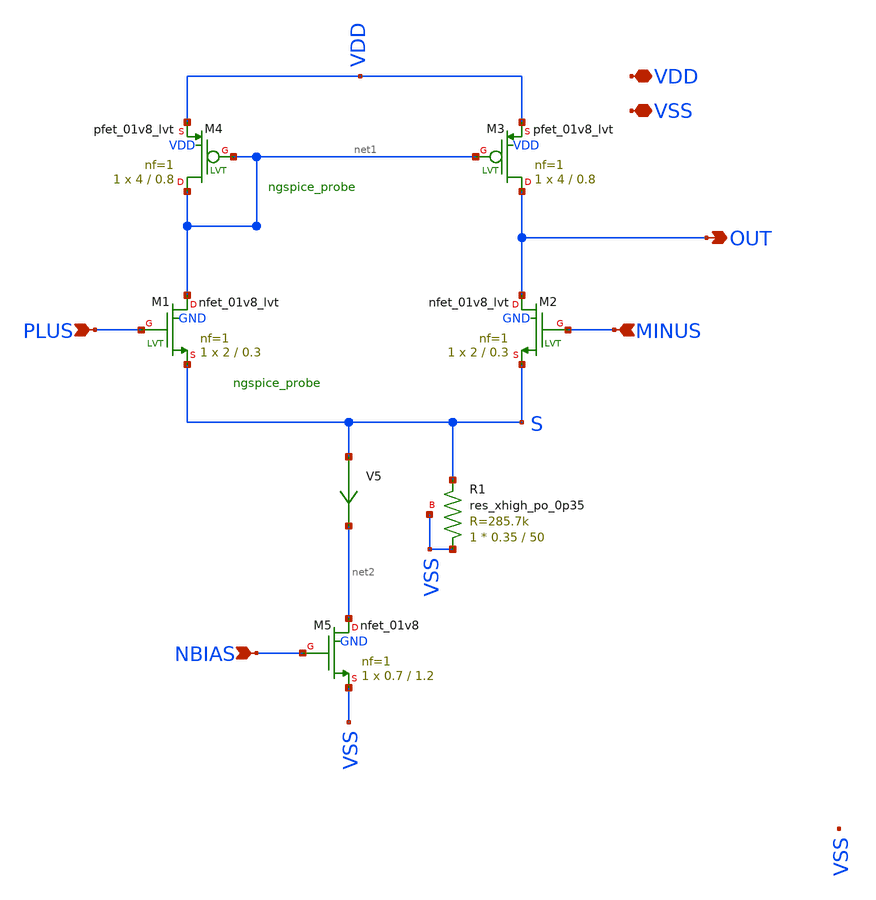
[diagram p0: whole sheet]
** sch_path: xschem/n_diffamp.sch
* Copyright 2021 Stefan Frederik Schippers
* Licensed under the Apache License, Version 2.0 (the "License");
* you may not use this file except in compliance with the License.
* You may obtain a copy of the License at
* https://www.apache.org/licenses/LICENSE-2.0
* Unless required by applicable law or agreed to in writing, software
* distributed under the License is distributed on an "AS IS" BASIS,
* WITHOUT WARRANTIES OR CONDITIONS OF ANY KIND, either express or implied.
* See the License for the specific language governing permissions and
* limitations under the License.
**.subckt n_diffamp PLUS MINUS OUT NBIAS VDD VSS
*.ipin PLUS
*.ipin MINUS
*.opin OUT
*.ipin NBIAS
*.iopin VDD
*.iopin VSS
XM1 net1 PLUS S GND sky130_fd_pr__nfet_01v8_lvt L=0.3 W=2 nf=1 ad='int((nf+1)/2) * W/nf * 0.29' as='int((nf+2)/2) * W/nf * 0.29'
+ pd='2*int((nf+1)/2) * (W/nf + 0.29)' ps='2*int((nf+2)/2) * (W/nf + 0.29)' nrd='0.29 / W' nrs='0.29 / W'
+ sa=0 sb=0 sd=0 mult=1 m=1
XM2 OUT MINUS S GND sky130_fd_pr__nfet_01v8_lvt L=0.3 W=2 nf=1 ad='int((nf+1)/2) * W/nf * 0.29' as='int((nf+2)/2) * W/nf * 0.29'
+ pd='2*int((nf+1)/2) * (W/nf + 0.29)' ps='2*int((nf+2)/2) * (W/nf + 0.29)' nrd='0.29 / W' nrs='0.29 / W'
+ sa=0 sb=0 sd=0 mult=1 m=1
XM3 OUT net1 VDD VDD sky130_fd_pr__pfet_01v8_lvt L=0.8 W=4 nf=1 ad='int((nf+1)/2) * W/nf * 0.29' as='int((nf+2)/2) * W/nf * 0.29'
+ pd='2*int((nf+1)/2) * (W/nf + 0.29)' ps='2*int((nf+2)/2) * (W/nf + 0.29)' nrd='0.29 / W' nrs='0.29 / W'
+ sa=0 sb=0 sd=0 mult=1 m=1
XM4 net1 net1 VDD VDD sky130_fd_pr__pfet_01v8_lvt L=0.8 W=4 nf=1 ad='int((nf+1)/2) * W/nf * 0.29' as='int((nf+2)/2) * W/nf * 0.29'
+ pd='2*int((nf+1)/2) * (W/nf + 0.29)' ps='2*int((nf+2)/2) * (W/nf + 0.29)' nrd='0.29 / W' nrs='0.29 / W'
+ sa=0 sb=0 sd=0 mult=1 m=1
XM5 net2 NBIAS VSS GND sky130_fd_pr__nfet_01v8 L=1.2 W=0.7 nf=1 ad='int((nf+1)/2) * W/nf * 0.29' as='int((nf+2)/2) * W/nf * 0.29'
+ pd='2*int((nf+1)/2) * (W/nf + 0.29)' ps='2*int((nf+2)/2) * (W/nf + 0.29)' nrd='0.29 / W' nrs='0.29 / W'
+ sa=0 sb=0 sd=0 mult=1 m=1
XR1 VSS S VSS sky130_fd_pr__res_xhigh_po_0p35 L=50 mult=1 m=1
V5 S net2 0
.save i(v5)
**.ends
.end
